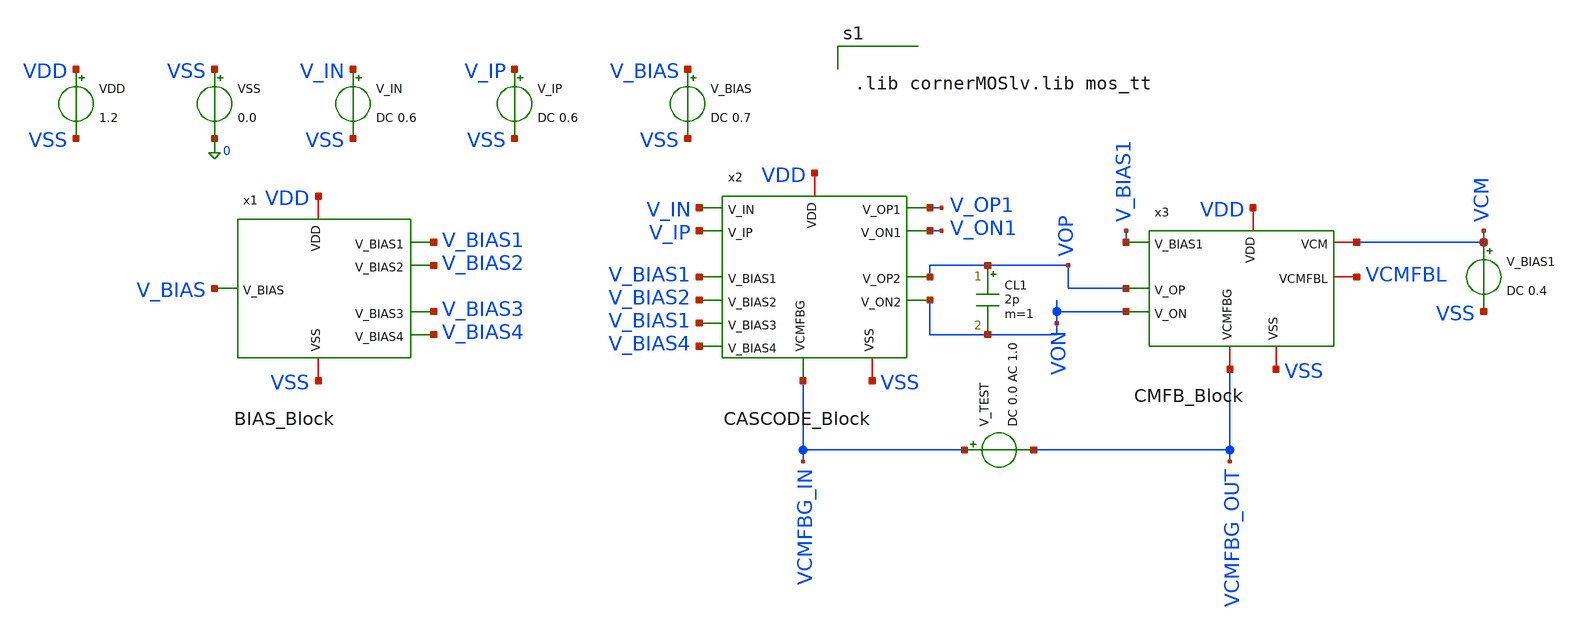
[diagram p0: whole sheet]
** sch_path: two-stage-ota-with-cmfb/Simulation/TEST_CMFB.sch
**.subckt TEST_CMFB
VDD VDD VSS 1.2
VSS VSS 0 0.0
V_IN V_IN VSS DC 0.6
V_IP V_IP VSS DC 0.6
V_BIAS V_BIAS VSS DC 0.7
V_BIAS1 VCM VSS DC 0.4
CL1 VOP VON 2p m=1
x1 VSS V_BIAS4 V_BIAS2 V_BIAS3 VDD V_BIAS1 V_BIAS BIAS_Block
x2 VDD V_BIAS1 V_IN V_IP V_BIAS2 V_ON1 V_OP1 V_BIAS1 VON VOP VCMFBG_IN V_BIAS4 VSS CASCODE_Block
x3 VDD V_BIAS1 VCM VOP VON VCMFBL VCMFBG_OUT VSS CMFB_Block
V_TEST VCMFBG_IN VCMFBG_OUT DC 0.0 AC 1.0
**** begin user architecture code


.lib cornerMOSlv.lib mos_tt




* ==============================================================================
* MUC E: CMFB LOOP STABILITY ANALYSIS
* ==============================================================================

.control
set color0=white
set color1=black

echo '=========================================================================='
echo '  E. CMFB LOOP GAIN & PHASE MARGIN SIMULATION                           '
echo '=========================================================================='

* 1. Chay AC sweep tu 1 Hz den 10 GHz, 20 diem moi decade
ac dec 20 1 10G

* 2. Tinh toan Loop Gain va Phase cua vong CMFB
* Dau am (-) the hien vong hoi tiep am
let t_cmfb = - v(vcmfbg_out) / v(vcmfbg_in)
let cmfb_gain_db = db(t_cmfb)
let cmfb_phase   = (cph(t_cmfb) * 180 / pi)

* Hieu chinh pha ve dai [-180, 180] de de doc Phase Margin
* Phase Margin (PM) do tai tan so cat Unity-Gain Frequency (khi Gain = 0 dB)
* PM = Phase + 180 (neu pha bat dau tu -180) hoac PM = Phase (neu pha bat dau tu 0)

* --- DO DC LOOP GAIN (tai 1 Hz) ---
meas ac cmfb_dc_gain find cmfb_gain_db at=1

* --- DO UNITY-GAIN FREQUENCY (UGBW cua vong CMFB, tai Gain = 0 dB) ---
meas ac f_ugbw when cmfb_gain_db=0 fall=1

* --- DO PHASE MARGIN ---
meas ac phase_at_ugbw find cmfb_phase when cmfb_gain_db=0 fall=1
let cmfb_pm = 180 + phase_at_ugbw

echo '--------------------------------------------------------------------------'
echo 'KET QUA DO VONG HOI TIEP CMFB:'
echo '--------------------------------------------------------------------------'
print cmfb_dc_gain
print f_ugbw
print cmfb_pm
echo '--------------------------------------------------------------------------'

* 3. Ve bieu do Bode (Bien do va Pha) cua vong CMFB
plot cmfb_gain_db ylabel 'Loop Gain (dB)' xlabel 'Frequency (Hz)' title 'CMFB Open-Loop Gain vs. Frequency'
plot cmfb_phase ylabel 'Phase (degrees)' xlabel 'Time/Freq (Hz)' title 'CMFB Open-Loop Phase vs. Frequency'

.endc


**** end user architecture code
**.ends
.end
